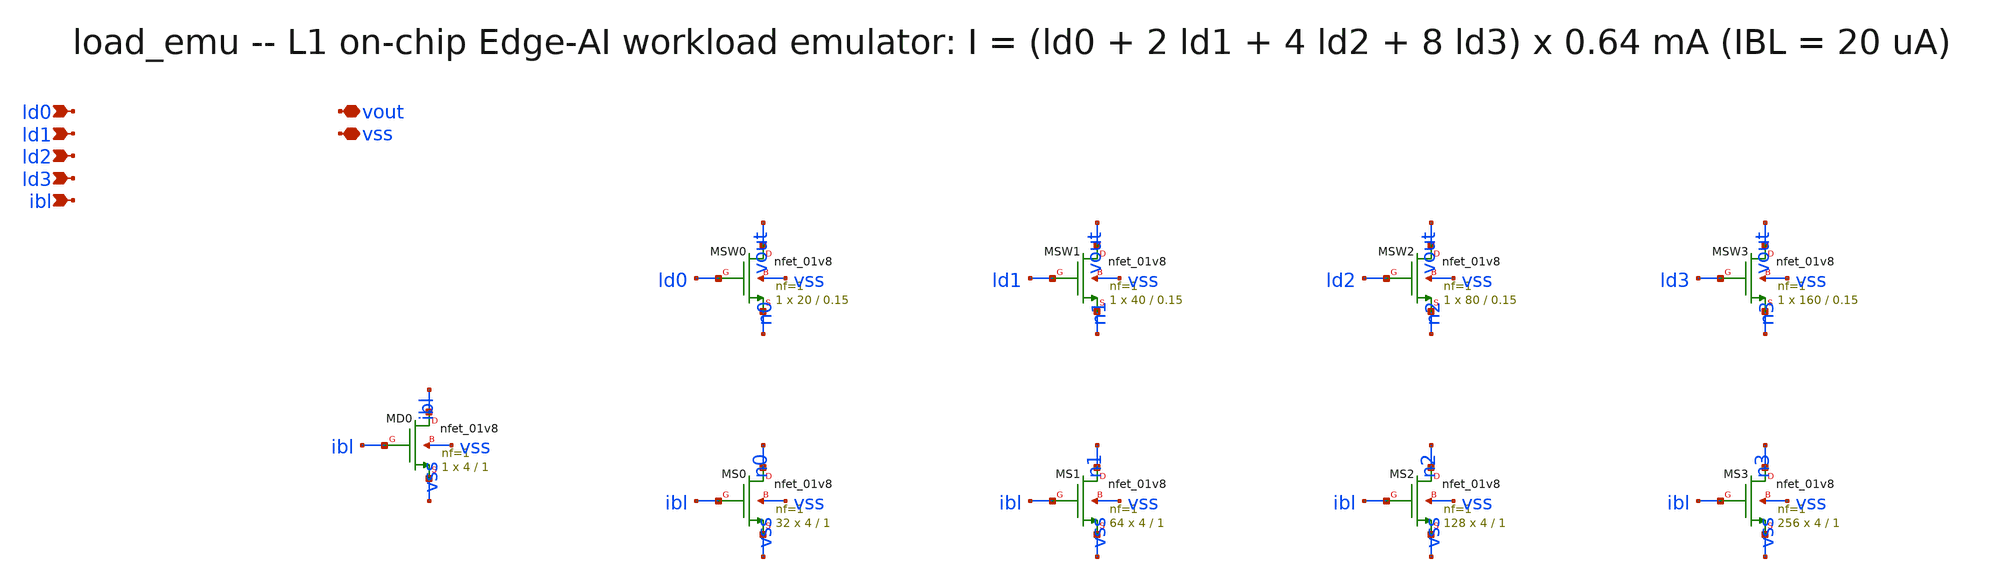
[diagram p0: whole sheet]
** sch_path: xschem/onetops/load_emu.sch
**.subckt load_emu ld0 ld1 ld2 ld3 ibl vout vss
*.ipin ld0
*.ipin ld1
*.ipin ld2
*.ipin ld3
*.ipin ibl
*.iopin vout
*.iopin vss
XMD0 ibl ibl vss vss sky130_fd_pr__nfet_01v8 L=1 W=4 nf=1 ad='int((1 + 1)/2) * 4 / 1 * 0.29' as='int((1 + 2)/2) * 4 / 1 * 0.29'
+ pd='2*int((1 + 1)/2) * (4 / 1 + 0.29)' ps='2*int((1 + 2)/2) * (4 / 1 + 0.29)' nrd='0.29 / 4 ' nrs='0.29 / 4 '
+ sa=0 sb=0 sd=0 mult=1 m=1
XMSW0 vout ld0 n0 vss sky130_fd_pr__nfet_01v8 L=0.15 W=20 nf=1 ad='int((1 + 1)/2) * 20 / 1 * 0.29' as='int((1 + 2)/2) * 20 / 1 * 0.29'
+ pd='2*int((1 + 1)/2) * (20 / 1 + 0.29)' ps='2*int((1 + 2)/2) * (20 / 1 + 0.29)' nrd='0.29 / 20 ' nrs='0.29 / 20 '
+ sa=0 sb=0 sd=0 mult=1 m=1
XMS0 n0 ibl vss vss sky130_fd_pr__nfet_01v8 L=1 W=4 nf=1 ad='int((1 + 1)/2) * 4 / 1 * 0.29' as='int((1 + 2)/2) * 4 / 1 * 0.29'
+ pd='2*int((1 + 1)/2) * (4 / 1 + 0.29)' ps='2*int((1 + 2)/2) * (4 / 1 + 0.29)' nrd='0.29 / 4 ' nrs='0.29 / 4 '
+ sa=0 sb=0 sd=0 mult=32 m=32
XMSW1 vout ld1 n1 vss sky130_fd_pr__nfet_01v8 L=0.15 W=40 nf=1 ad='int((1 + 1)/2) * 40 / 1 * 0.29' as='int((1 + 2)/2) * 40 / 1 * 0.29'
+ pd='2*int((1 + 1)/2) * (40 / 1 + 0.29)' ps='2*int((1 + 2)/2) * (40 / 1 + 0.29)' nrd='0.29 / 40 ' nrs='0.29 / 40 '
+ sa=0 sb=0 sd=0 mult=1 m=1
XMS1 n1 ibl vss vss sky130_fd_pr__nfet_01v8 L=1 W=4 nf=1 ad='int((1 + 1)/2) * 4 / 1 * 0.29' as='int((1 + 2)/2) * 4 / 1 * 0.29'
+ pd='2*int((1 + 1)/2) * (4 / 1 + 0.29)' ps='2*int((1 + 2)/2) * (4 / 1 + 0.29)' nrd='0.29 / 4 ' nrs='0.29 / 4 '
+ sa=0 sb=0 sd=0 mult=64 m=64
XMSW2 vout ld2 n2 vss sky130_fd_pr__nfet_01v8 L=0.15 W=80 nf=1 ad='int((1 + 1)/2) * 80 / 1 * 0.29' as='int((1 + 2)/2) * 80 / 1 * 0.29'
+ pd='2*int((1 + 1)/2) * (80 / 1 + 0.29)' ps='2*int((1 + 2)/2) * (80 / 1 + 0.29)' nrd='0.29 / 80 ' nrs='0.29 / 80 '
+ sa=0 sb=0 sd=0 mult=1 m=1
XMS2 n2 ibl vss vss sky130_fd_pr__nfet_01v8 L=1 W=4 nf=1 ad='int((1 + 1)/2) * 4 / 1 * 0.29' as='int((1 + 2)/2) * 4 / 1 * 0.29'
+ pd='2*int((1 + 1)/2) * (4 / 1 + 0.29)' ps='2*int((1 + 2)/2) * (4 / 1 + 0.29)' nrd='0.29 / 4 ' nrs='0.29 / 4 '
+ sa=0 sb=0 sd=0 mult=128 m=128
XMSW3 vout ld3 n3 vss sky130_fd_pr__nfet_01v8 L=0.15 W=160 nf=1 ad='int((1 + 1)/2) * 160 / 1 * 0.29'
+ as='int((1 + 2)/2) * 160 / 1 * 0.29' pd='2*int((1 + 1)/2) * (160 / 1 + 0.29)' ps='2*int((1 + 2)/2) * (160 / 1 + 0.29)'
+ nrd='0.29 / 160 ' nrs='0.29 / 160 ' sa=0 sb=0 sd=0 mult=1 m=1
XMS3 n3 ibl vss vss sky130_fd_pr__nfet_01v8 L=1 W=4 nf=1 ad='int((1 + 1)/2) * 4 / 1 * 0.29' as='int((1 + 2)/2) * 4 / 1 * 0.29'
+ pd='2*int((1 + 1)/2) * (4 / 1 + 0.29)' ps='2*int((1 + 2)/2) * (4 / 1 + 0.29)' nrd='0.29 / 4 ' nrs='0.29 / 4 '
+ sa=0 sb=0 sd=0 mult=256 m=256
**.ends
.end
